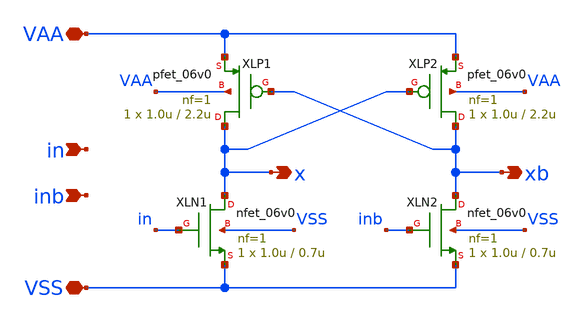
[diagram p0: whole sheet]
** sch_path: xschem/ck_LS.sch
**.subckt ck_LS in inb x xb VSS VAA
*.ipin in
*.ipin inb
*.opin x
*.opin xb
*.iopin VSS
*.iopin VAA
XLP1 x xb VAA VAA pfet_06v0 L=2.2u W=1.0u nf=1 ad='int((nf+1)/2) * W/nf * 0.18u' as='int((nf+2)/2) * W/nf * 0.18u'
+ pd='2*int((nf+1)/2) * (W/nf + 0.18u)' ps='2*int((nf+2)/2) * (W/nf + 0.18u)' nrd='0.18u / W' nrs='0.18u / W'
+ sa=0 sb=0 sd=0 m=1
XLP2 xb x VAA VAA pfet_06v0 L=2.2u W=1.0u nf=1 ad='int((nf+1)/2) * W/nf * 0.18u' as='int((nf+2)/2) * W/nf * 0.18u'
+ pd='2*int((nf+1)/2) * (W/nf + 0.18u)' ps='2*int((nf+2)/2) * (W/nf + 0.18u)' nrd='0.18u / W' nrs='0.18u / W'
+ sa=0 sb=0 sd=0 m=1
XLN1 x in VSS VSS nfet_06v0 L=0.7u W=1.0u nf=1 ad='int((nf+1)/2) * W/nf * 0.18u' as='int((nf+2)/2) * W/nf * 0.18u'
+ pd='2*int((nf+1)/2) * (W/nf + 0.18u)' ps='2*int((nf+2)/2) * (W/nf + 0.18u)' nrd='0.18u / W' nrs='0.18u / W'
+ sa=0 sb=0 sd=0 m=1 par=1
XLN2 xb inb VSS VSS nfet_06v0 L=0.7u W=1.0u nf=1 ad='int((nf+1)/2) * W/nf * 0.18u' as='int((nf+2)/2) * W/nf * 0.18u'
+ pd='2*int((nf+1)/2) * (W/nf + 0.18u)' ps='2*int((nf+2)/2) * (W/nf + 0.18u)' nrd='0.18u / W' nrs='0.18u / W'
+ sa=0 sb=0 sd=0 m=1 par=1
**.ends
.end
